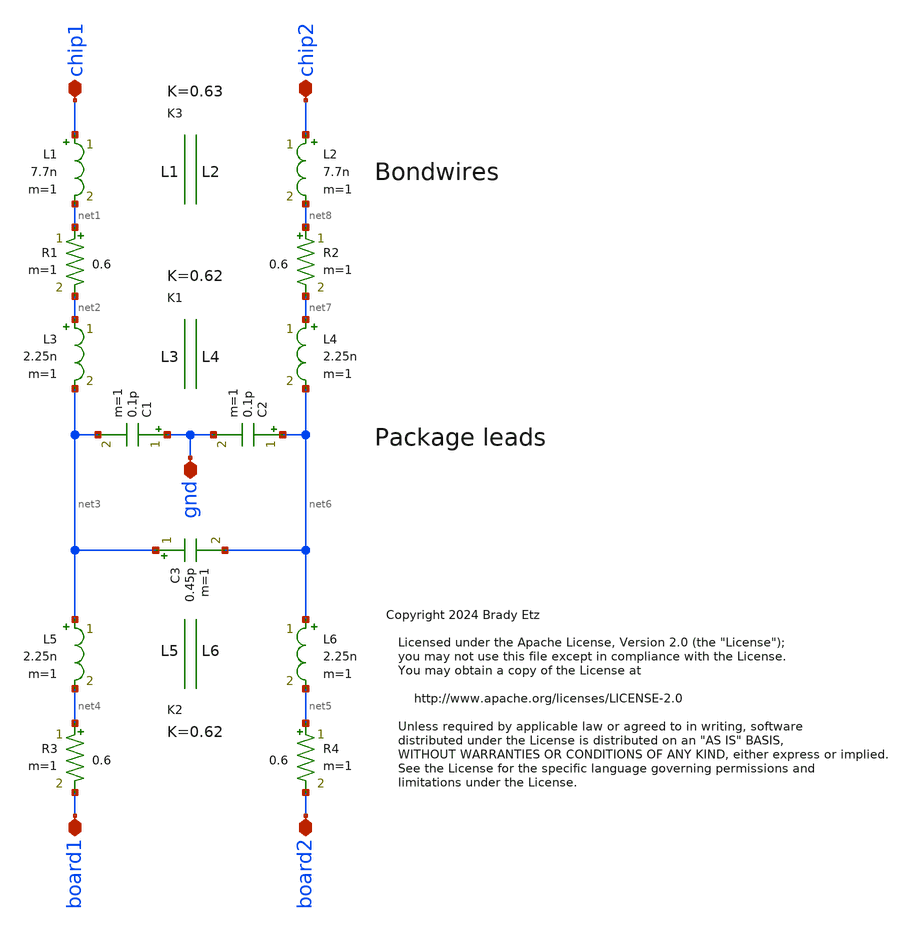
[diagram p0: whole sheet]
** sch_path: xschem/lqfp_parasitics.sch
* Copyright 2024 Brady Etz
* Licensed under the Apache License, Version 2.0 (the "License");
**.subckt lqfp_parasitics chip1 chip2 board2 board1 gnd
*.iopin chip1
*.iopin chip2
*.iopin board2
*.iopin board1
*.iopin gnd
L5 net3 net4 2.25n m=1
L6 net6 net5 2.25n m=1
K1 L3 L4 0.62
L3 net2 net3 2.25n m=1
L4 net7 net6 2.25n m=1
C3 net3 net6 0.45p m=1
C2 net6 gnd 0.1p m=1
C1 gnd net3 0.1p m=1
R4 net5 board2 0.6 m=1
R3 net4 board1 0.6 m=1
K2 L5 L6 0.62
R2 net8 net7 0.6 m=1
R1 net1 net2 0.6 m=1
L1 chip1 net1 7.7n m=1
L2 chip2 net8 7.7n m=1
K3 L1 L2 0.63
**.ends
.end
